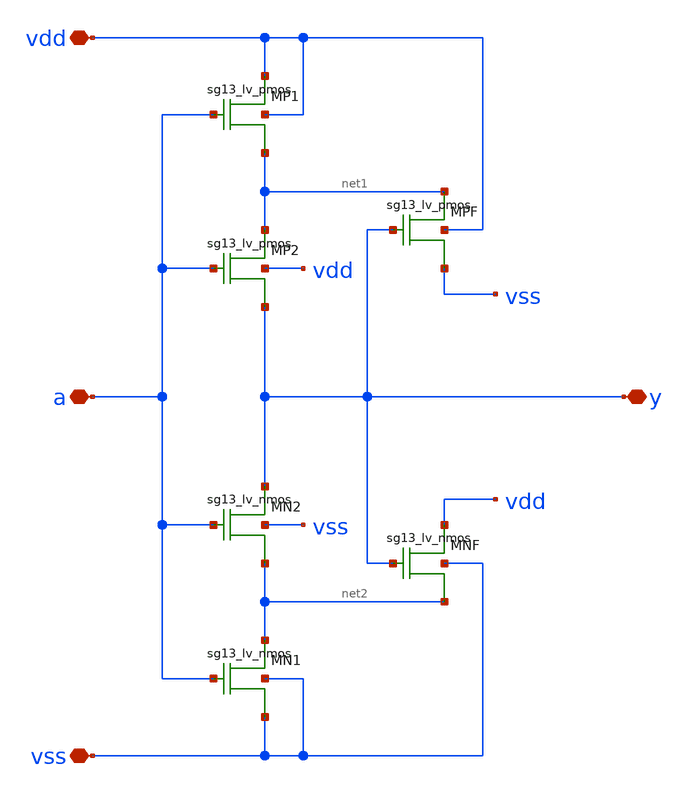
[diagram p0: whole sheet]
** sch_path: xschem/logic_gates/SCHMLV.sch
**.subckt SCHMLV vdd vss y a
*.iopin vdd
*.iopin vss
*.iopin y
*.iopin a
XMP1 vdd a net1 vdd sg13_lv_pmos w=2.0u l=0.13u ng=1 m=1
XMP2 net1 a y vdd sg13_lv_pmos w=2.0u l=0.13u ng=1 m=1
XMN2 y a net2 vss sg13_lv_nmos w=1.0u l=0.13u ng=1 m=1
XMN1 net2 a vss vss sg13_lv_nmos w=1.0u l=0.13u ng=1 m=1
XMPF net1 y vss vdd sg13_lv_pmos w=1.2u l=0.13u ng=1 m=1
XMNF vdd y net2 vss sg13_lv_nmos w=0.6u l=0.13u ng=1 m=1
**.ends
.end
